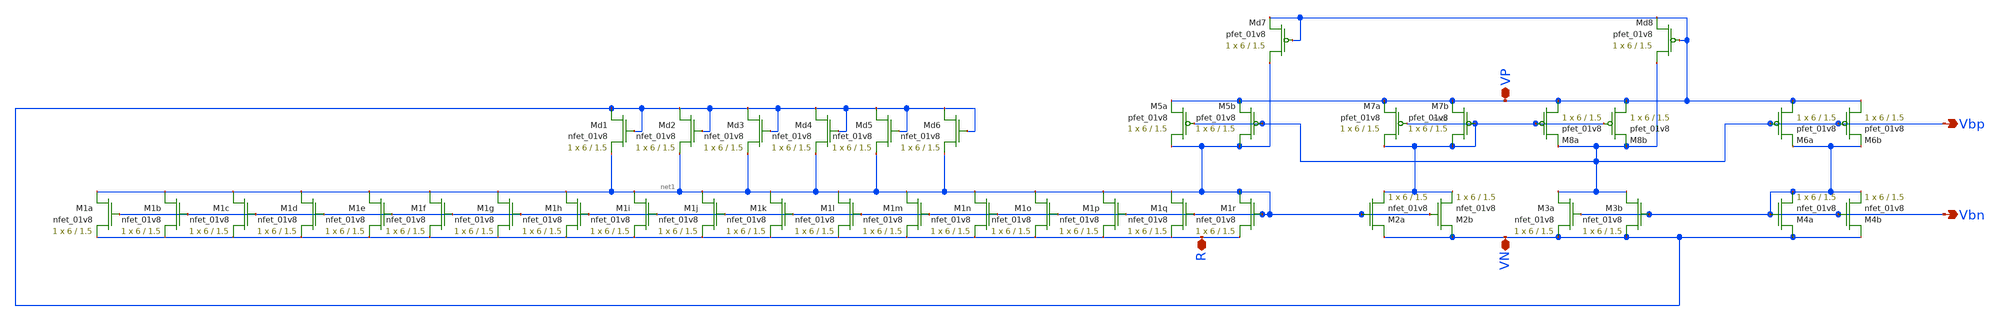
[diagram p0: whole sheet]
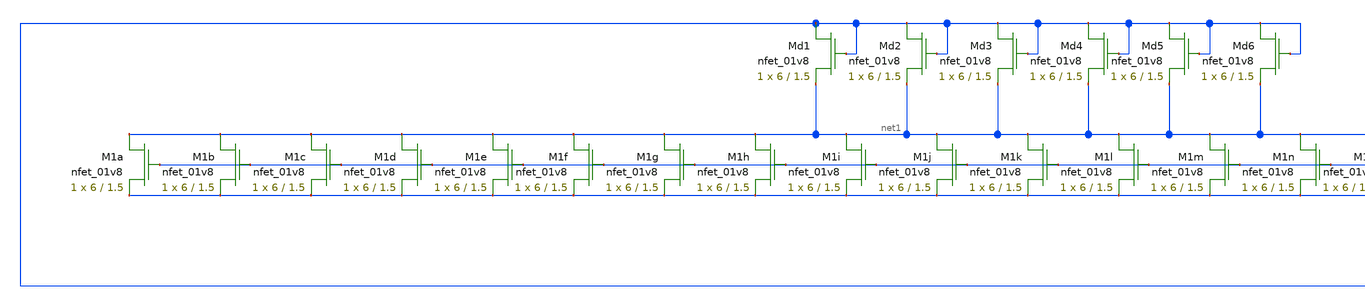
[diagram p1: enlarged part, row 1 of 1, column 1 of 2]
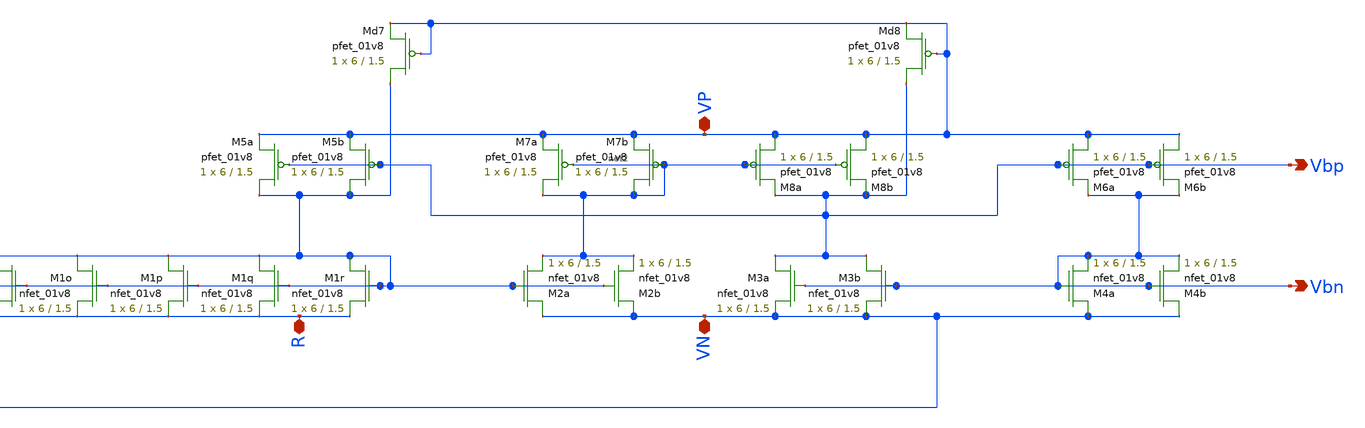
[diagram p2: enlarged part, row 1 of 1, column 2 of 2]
** sch_path: schematics/bias/current_bias_for_lvs.sch
**.subckt current_bias_for_lvs VN VP Vbn Vbp R
*.iopin VN
*.iopin VP
*.opin Vbn
*.opin Vbp
*.iopin R
XM5a net1 Vbp VP VDD sky130_fd_pr__pfet_01v8 L=1.5 W=6 nf=1 ad='int((nf+1)/2) * W/nf * 0.29' as='int((nf+2)/2) * W/nf * 0.29'
+ pd='2*int((nf+1)/2) * (W/nf + 0.29)' ps='2*int((nf+2)/2) * (W/nf + 0.29)' nrd='0.29 / W' nrs='0.29 / W'
+ sa=0 sb=0 sd=0 mult=1 m=1
XM5b net1 Vbp VP VDD sky130_fd_pr__pfet_01v8 L=1.5 W=6 nf=1 ad='int((nf+1)/2) * W/nf * 0.29' as='int((nf+2)/2) * W/nf * 0.29'
+ pd='2*int((nf+1)/2) * (W/nf + 0.29)' ps='2*int((nf+2)/2) * (W/nf + 0.29)' nrd='0.29 / W' nrs='0.29 / W'
+ sa=0 sb=0 sd=0 mult=1 m=1
XM1i net1 net1 R GND sky130_fd_pr__nfet_01v8 L=1.5 W=6 nf=1 ad='int((nf+1)/2) * W/nf * 0.29' as='int((nf+2)/2) * W/nf * 0.29'
+ pd='2*int((nf+1)/2) * (W/nf + 0.29)' ps='2*int((nf+2)/2) * (W/nf + 0.29)' nrd='0.29 / W' nrs='0.29 / W'
+ sa=0 sb=0 sd=0 mult=1 m=1
XM1h net1 net1 R GND sky130_fd_pr__nfet_01v8 L=1.5 W=6 nf=1 ad='int((nf+1)/2) * W/nf * 0.29' as='int((nf+2)/2) * W/nf * 0.29'
+ pd='2*int((nf+1)/2) * (W/nf + 0.29)' ps='2*int((nf+2)/2) * (W/nf + 0.29)' nrd='0.29 / W' nrs='0.29 / W'
+ sa=0 sb=0 sd=0 mult=1 m=1
XM1g net1 net1 R GND sky130_fd_pr__nfet_01v8 L=1.5 W=6 nf=1 ad='int((nf+1)/2) * W/nf * 0.29' as='int((nf+2)/2) * W/nf * 0.29'
+ pd='2*int((nf+1)/2) * (W/nf + 0.29)' ps='2*int((nf+2)/2) * (W/nf + 0.29)' nrd='0.29 / W' nrs='0.29 / W'
+ sa=0 sb=0 sd=0 mult=1 m=1
XM1f net1 net1 R GND sky130_fd_pr__nfet_01v8 L=1.5 W=6 nf=1 ad='int((nf+1)/2) * W/nf * 0.29' as='int((nf+2)/2) * W/nf * 0.29'
+ pd='2*int((nf+1)/2) * (W/nf + 0.29)' ps='2*int((nf+2)/2) * (W/nf + 0.29)' nrd='0.29 / W' nrs='0.29 / W'
+ sa=0 sb=0 sd=0 mult=1 m=1
XM1e net1 net1 R GND sky130_fd_pr__nfet_01v8 L=1.5 W=6 nf=1 ad='int((nf+1)/2) * W/nf * 0.29' as='int((nf+2)/2) * W/nf * 0.29'
+ pd='2*int((nf+1)/2) * (W/nf + 0.29)' ps='2*int((nf+2)/2) * (W/nf + 0.29)' nrd='0.29 / W' nrs='0.29 / W'
+ sa=0 sb=0 sd=0 mult=1 m=1
XM1d net1 net1 R GND sky130_fd_pr__nfet_01v8 L=1.5 W=6 nf=1 ad='int((nf+1)/2) * W/nf * 0.29' as='int((nf+2)/2) * W/nf * 0.29'
+ pd='2*int((nf+1)/2) * (W/nf + 0.29)' ps='2*int((nf+2)/2) * (W/nf + 0.29)' nrd='0.29 / W' nrs='0.29 / W'
+ sa=0 sb=0 sd=0 mult=1 m=1
XM1c net1 net1 R GND sky130_fd_pr__nfet_01v8 L=1.5 W=6 nf=1 ad='int((nf+1)/2) * W/nf * 0.29' as='int((nf+2)/2) * W/nf * 0.29'
+ pd='2*int((nf+1)/2) * (W/nf + 0.29)' ps='2*int((nf+2)/2) * (W/nf + 0.29)' nrd='0.29 / W' nrs='0.29 / W'
+ sa=0 sb=0 sd=0 mult=1 m=1
XM1b net1 net1 R GND sky130_fd_pr__nfet_01v8 L=1.5 W=6 nf=1 ad='int((nf+1)/2) * W/nf * 0.29' as='int((nf+2)/2) * W/nf * 0.29'
+ pd='2*int((nf+1)/2) * (W/nf + 0.29)' ps='2*int((nf+2)/2) * (W/nf + 0.29)' nrd='0.29 / W' nrs='0.29 / W'
+ sa=0 sb=0 sd=0 mult=1 m=1
XM1a net1 net1 R GND sky130_fd_pr__nfet_01v8 L=1.5 W=6 nf=1 ad='int((nf+1)/2) * W/nf * 0.29' as='int((nf+2)/2) * W/nf * 0.29'
+ pd='2*int((nf+1)/2) * (W/nf + 0.29)' ps='2*int((nf+2)/2) * (W/nf + 0.29)' nrd='0.29 / W' nrs='0.29 / W'
+ sa=0 sb=0 sd=0 mult=1 m=1
XM7a net2 net2 VP VDD sky130_fd_pr__pfet_01v8 L=1.5 W=6 nf=1 ad='int((nf+1)/2) * W/nf * 0.29' as='int((nf+2)/2) * W/nf * 0.29'
+ pd='2*int((nf+1)/2) * (W/nf + 0.29)' ps='2*int((nf+2)/2) * (W/nf + 0.29)' nrd='0.29 / W' nrs='0.29 / W'
+ sa=0 sb=0 sd=0 mult=1 m=1
XM7b net2 net2 VP VDD sky130_fd_pr__pfet_01v8 L=1.5 W=6 nf=1 ad='int((nf+1)/2) * W/nf * 0.29' as='int((nf+2)/2) * W/nf * 0.29'
+ pd='2*int((nf+1)/2) * (W/nf + 0.29)' ps='2*int((nf+2)/2) * (W/nf + 0.29)' nrd='0.29 / W' nrs='0.29 / W'
+ sa=0 sb=0 sd=0 mult=1 m=1
XM8b VP net2 Vbp VDD sky130_fd_pr__pfet_01v8 L=1.5 W=6 nf=1 ad='int((nf+1)/2) * W/nf * 0.29' as='int((nf+2)/2) * W/nf * 0.29'
+ pd='2*int((nf+1)/2) * (W/nf + 0.29)' ps='2*int((nf+2)/2) * (W/nf + 0.29)' nrd='0.29 / W' nrs='0.29 / W'
+ sa=0 sb=0 sd=0 mult=1 m=1
XM8a VP net2 Vbp VDD sky130_fd_pr__pfet_01v8 L=1.5 W=6 nf=1 ad='int((nf+1)/2) * W/nf * 0.29' as='int((nf+2)/2) * W/nf * 0.29'
+ pd='2*int((nf+1)/2) * (W/nf + 0.29)' ps='2*int((nf+2)/2) * (W/nf + 0.29)' nrd='0.29 / W' nrs='0.29 / W'
+ sa=0 sb=0 sd=0 mult=1 m=1
XM6b VP Vbp Vbn VDD sky130_fd_pr__pfet_01v8 L=1.5 W=6 nf=1 ad='int((nf+1)/2) * W/nf * 0.29' as='int((nf+2)/2) * W/nf * 0.29'
+ pd='2*int((nf+1)/2) * (W/nf + 0.29)' ps='2*int((nf+2)/2) * (W/nf + 0.29)' nrd='0.29 / W' nrs='0.29 / W'
+ sa=0 sb=0 sd=0 mult=1 m=1
XM6a VP Vbp Vbn VDD sky130_fd_pr__pfet_01v8 L=1.5 W=6 nf=1 ad='int((nf+1)/2) * W/nf * 0.29' as='int((nf+2)/2) * W/nf * 0.29'
+ pd='2*int((nf+1)/2) * (W/nf + 0.29)' ps='2*int((nf+2)/2) * (W/nf + 0.29)' nrd='0.29 / W' nrs='0.29 / W'
+ sa=0 sb=0 sd=0 mult=1 m=1
XM2a VN net1 net2 GND sky130_fd_pr__nfet_01v8 L=1.5 W=6 nf=1 ad='int((nf+1)/2) * W/nf * 0.29' as='int((nf+2)/2) * W/nf * 0.29'
+ pd='2*int((nf+1)/2) * (W/nf + 0.29)' ps='2*int((nf+2)/2) * (W/nf + 0.29)' nrd='0.29 / W' nrs='0.29 / W'
+ sa=0 sb=0 sd=0 mult=1 m=1
XM2b VN net1 net2 GND sky130_fd_pr__nfet_01v8 L=1.5 W=6 nf=1 ad='int((nf+1)/2) * W/nf * 0.29' as='int((nf+2)/2) * W/nf * 0.29'
+ pd='2*int((nf+1)/2) * (W/nf + 0.29)' ps='2*int((nf+2)/2) * (W/nf + 0.29)' nrd='0.29 / W' nrs='0.29 / W'
+ sa=0 sb=0 sd=0 mult=1 m=1
XM3b Vbp Vbn VN GND sky130_fd_pr__nfet_01v8 L=1.5 W=6 nf=1 ad='int((nf+1)/2) * W/nf * 0.29' as='int((nf+2)/2) * W/nf * 0.29'
+ pd='2*int((nf+1)/2) * (W/nf + 0.29)' ps='2*int((nf+2)/2) * (W/nf + 0.29)' nrd='0.29 / W' nrs='0.29 / W'
+ sa=0 sb=0 sd=0 mult=1 m=1
XM3a Vbp Vbn VN GND sky130_fd_pr__nfet_01v8 L=1.5 W=6 nf=1 ad='int((nf+1)/2) * W/nf * 0.29' as='int((nf+2)/2) * W/nf * 0.29'
+ pd='2*int((nf+1)/2) * (W/nf + 0.29)' ps='2*int((nf+2)/2) * (W/nf + 0.29)' nrd='0.29 / W' nrs='0.29 / W'
+ sa=0 sb=0 sd=0 mult=1 m=1
XM4a VN Vbn Vbn GND sky130_fd_pr__nfet_01v8 L=1.5 W=6 nf=1 ad='int((nf+1)/2) * W/nf * 0.29' as='int((nf+2)/2) * W/nf * 0.29'
+ pd='2*int((nf+1)/2) * (W/nf + 0.29)' ps='2*int((nf+2)/2) * (W/nf + 0.29)' nrd='0.29 / W' nrs='0.29 / W'
+ sa=0 sb=0 sd=0 mult=1 m=1
XM4b VN Vbn Vbn GND sky130_fd_pr__nfet_01v8 L=1.5 W=6 nf=1 ad='int((nf+1)/2) * W/nf * 0.29' as='int((nf+2)/2) * W/nf * 0.29'
+ pd='2*int((nf+1)/2) * (W/nf + 0.29)' ps='2*int((nf+2)/2) * (W/nf + 0.29)' nrd='0.29 / W' nrs='0.29 / W'
+ sa=0 sb=0 sd=0 mult=1 m=1
XM1r net1 net1 R GND sky130_fd_pr__nfet_01v8 L=1.5 W=6 nf=1 ad='int((nf+1)/2) * W/nf * 0.29' as='int((nf+2)/2) * W/nf * 0.29'
+ pd='2*int((nf+1)/2) * (W/nf + 0.29)' ps='2*int((nf+2)/2) * (W/nf + 0.29)' nrd='0.29 / W' nrs='0.29 / W'
+ sa=0 sb=0 sd=0 mult=1 m=1
XM1q net1 net1 R GND sky130_fd_pr__nfet_01v8 L=1.5 W=6 nf=1 ad='int((nf+1)/2) * W/nf * 0.29' as='int((nf+2)/2) * W/nf * 0.29'
+ pd='2*int((nf+1)/2) * (W/nf + 0.29)' ps='2*int((nf+2)/2) * (W/nf + 0.29)' nrd='0.29 / W' nrs='0.29 / W'
+ sa=0 sb=0 sd=0 mult=1 m=1
XM1p net1 net1 R GND sky130_fd_pr__nfet_01v8 L=1.5 W=6 nf=1 ad='int((nf+1)/2) * W/nf * 0.29' as='int((nf+2)/2) * W/nf * 0.29'
+ pd='2*int((nf+1)/2) * (W/nf + 0.29)' ps='2*int((nf+2)/2) * (W/nf + 0.29)' nrd='0.29 / W' nrs='0.29 / W'
+ sa=0 sb=0 sd=0 mult=1 m=1
XM1o net1 net1 R GND sky130_fd_pr__nfet_01v8 L=1.5 W=6 nf=1 ad='int((nf+1)/2) * W/nf * 0.29' as='int((nf+2)/2) * W/nf * 0.29'
+ pd='2*int((nf+1)/2) * (W/nf + 0.29)' ps='2*int((nf+2)/2) * (W/nf + 0.29)' nrd='0.29 / W' nrs='0.29 / W'
+ sa=0 sb=0 sd=0 mult=1 m=1
XM1n net1 net1 R GND sky130_fd_pr__nfet_01v8 L=1.5 W=6 nf=1 ad='int((nf+1)/2) * W/nf * 0.29' as='int((nf+2)/2) * W/nf * 0.29'
+ pd='2*int((nf+1)/2) * (W/nf + 0.29)' ps='2*int((nf+2)/2) * (W/nf + 0.29)' nrd='0.29 / W' nrs='0.29 / W'
+ sa=0 sb=0 sd=0 mult=1 m=1
XM1m net1 net1 R GND sky130_fd_pr__nfet_01v8 L=1.5 W=6 nf=1 ad='int((nf+1)/2) * W/nf * 0.29' as='int((nf+2)/2) * W/nf * 0.29'
+ pd='2*int((nf+1)/2) * (W/nf + 0.29)' ps='2*int((nf+2)/2) * (W/nf + 0.29)' nrd='0.29 / W' nrs='0.29 / W'
+ sa=0 sb=0 sd=0 mult=1 m=1
XM1l net1 net1 R GND sky130_fd_pr__nfet_01v8 L=1.5 W=6 nf=1 ad='int((nf+1)/2) * W/nf * 0.29' as='int((nf+2)/2) * W/nf * 0.29'
+ pd='2*int((nf+1)/2) * (W/nf + 0.29)' ps='2*int((nf+2)/2) * (W/nf + 0.29)' nrd='0.29 / W' nrs='0.29 / W'
+ sa=0 sb=0 sd=0 mult=1 m=1
XM1k net1 net1 R GND sky130_fd_pr__nfet_01v8 L=1.5 W=6 nf=1 ad='int((nf+1)/2) * W/nf * 0.29' as='int((nf+2)/2) * W/nf * 0.29'
+ pd='2*int((nf+1)/2) * (W/nf + 0.29)' ps='2*int((nf+2)/2) * (W/nf + 0.29)' nrd='0.29 / W' nrs='0.29 / W'
+ sa=0 sb=0 sd=0 mult=1 m=1
XM1j net1 net1 R GND sky130_fd_pr__nfet_01v8 L=1.5 W=6 nf=1 ad='int((nf+1)/2) * W/nf * 0.29' as='int((nf+2)/2) * W/nf * 0.29'
+ pd='2*int((nf+1)/2) * (W/nf + 0.29)' ps='2*int((nf+2)/2) * (W/nf + 0.29)' nrd='0.29 / W' nrs='0.29 / W'
+ sa=0 sb=0 sd=0 mult=1 m=1
XMd1 VN VN net1 GND sky130_fd_pr__nfet_01v8 L=1.5 W=6 nf=1 ad='int((nf+1)/2) * W/nf * 0.29' as='int((nf+2)/2) * W/nf * 0.29'
+ pd='2*int((nf+1)/2) * (W/nf + 0.29)' ps='2*int((nf+2)/2) * (W/nf + 0.29)' nrd='0.29 / W' nrs='0.29 / W'
+ sa=0 sb=0 sd=0 mult=1 m=1
XMd2 VN VN net1 GND sky130_fd_pr__nfet_01v8 L=1.5 W=6 nf=1 ad='int((nf+1)/2) * W/nf * 0.29' as='int((nf+2)/2) * W/nf * 0.29'
+ pd='2*int((nf+1)/2) * (W/nf + 0.29)' ps='2*int((nf+2)/2) * (W/nf + 0.29)' nrd='0.29 / W' nrs='0.29 / W'
+ sa=0 sb=0 sd=0 mult=1 m=1
XMd3 VN VN net1 GND sky130_fd_pr__nfet_01v8 L=1.5 W=6 nf=1 ad='int((nf+1)/2) * W/nf * 0.29' as='int((nf+2)/2) * W/nf * 0.29'
+ pd='2*int((nf+1)/2) * (W/nf + 0.29)' ps='2*int((nf+2)/2) * (W/nf + 0.29)' nrd='0.29 / W' nrs='0.29 / W'
+ sa=0 sb=0 sd=0 mult=1 m=1
XMd4 VN VN net1 GND sky130_fd_pr__nfet_01v8 L=1.5 W=6 nf=1 ad='int((nf+1)/2) * W/nf * 0.29' as='int((nf+2)/2) * W/nf * 0.29'
+ pd='2*int((nf+1)/2) * (W/nf + 0.29)' ps='2*int((nf+2)/2) * (W/nf + 0.29)' nrd='0.29 / W' nrs='0.29 / W'
+ sa=0 sb=0 sd=0 mult=1 m=1
XMd5 VN VN net1 GND sky130_fd_pr__nfet_01v8 L=1.5 W=6 nf=1 ad='int((nf+1)/2) * W/nf * 0.29' as='int((nf+2)/2) * W/nf * 0.29'
+ pd='2*int((nf+1)/2) * (W/nf + 0.29)' ps='2*int((nf+2)/2) * (W/nf + 0.29)' nrd='0.29 / W' nrs='0.29 / W'
+ sa=0 sb=0 sd=0 mult=1 m=1
XMd6 VN VN net1 GND sky130_fd_pr__nfet_01v8 L=1.5 W=6 nf=1 ad='int((nf+1)/2) * W/nf * 0.29' as='int((nf+2)/2) * W/nf * 0.29'
+ pd='2*int((nf+1)/2) * (W/nf + 0.29)' ps='2*int((nf+2)/2) * (W/nf + 0.29)' nrd='0.29 / W' nrs='0.29 / W'
+ sa=0 sb=0 sd=0 mult=1 m=1
XMd7 net1 VP VP VDD sky130_fd_pr__pfet_01v8 L=1.5 W=6 nf=1 ad='int((nf+1)/2) * W/nf * 0.29' as='int((nf+2)/2) * W/nf * 0.29'
+ pd='2*int((nf+1)/2) * (W/nf + 0.29)' ps='2*int((nf+2)/2) * (W/nf + 0.29)' nrd='0.29 / W' nrs='0.29 / W'
+ sa=0 sb=0 sd=0 mult=1 m=1
XMd8 Vbp VP VP VDD sky130_fd_pr__pfet_01v8 L=1.5 W=6 nf=1 ad='int((nf+1)/2) * W/nf * 0.29' as='int((nf+2)/2) * W/nf * 0.29'
+ pd='2*int((nf+1)/2) * (W/nf + 0.29)' ps='2*int((nf+2)/2) * (W/nf + 0.29)' nrd='0.29 / W' nrs='0.29 / W'
+ sa=0 sb=0 sd=0 mult=1 m=1
**.ends
.end
